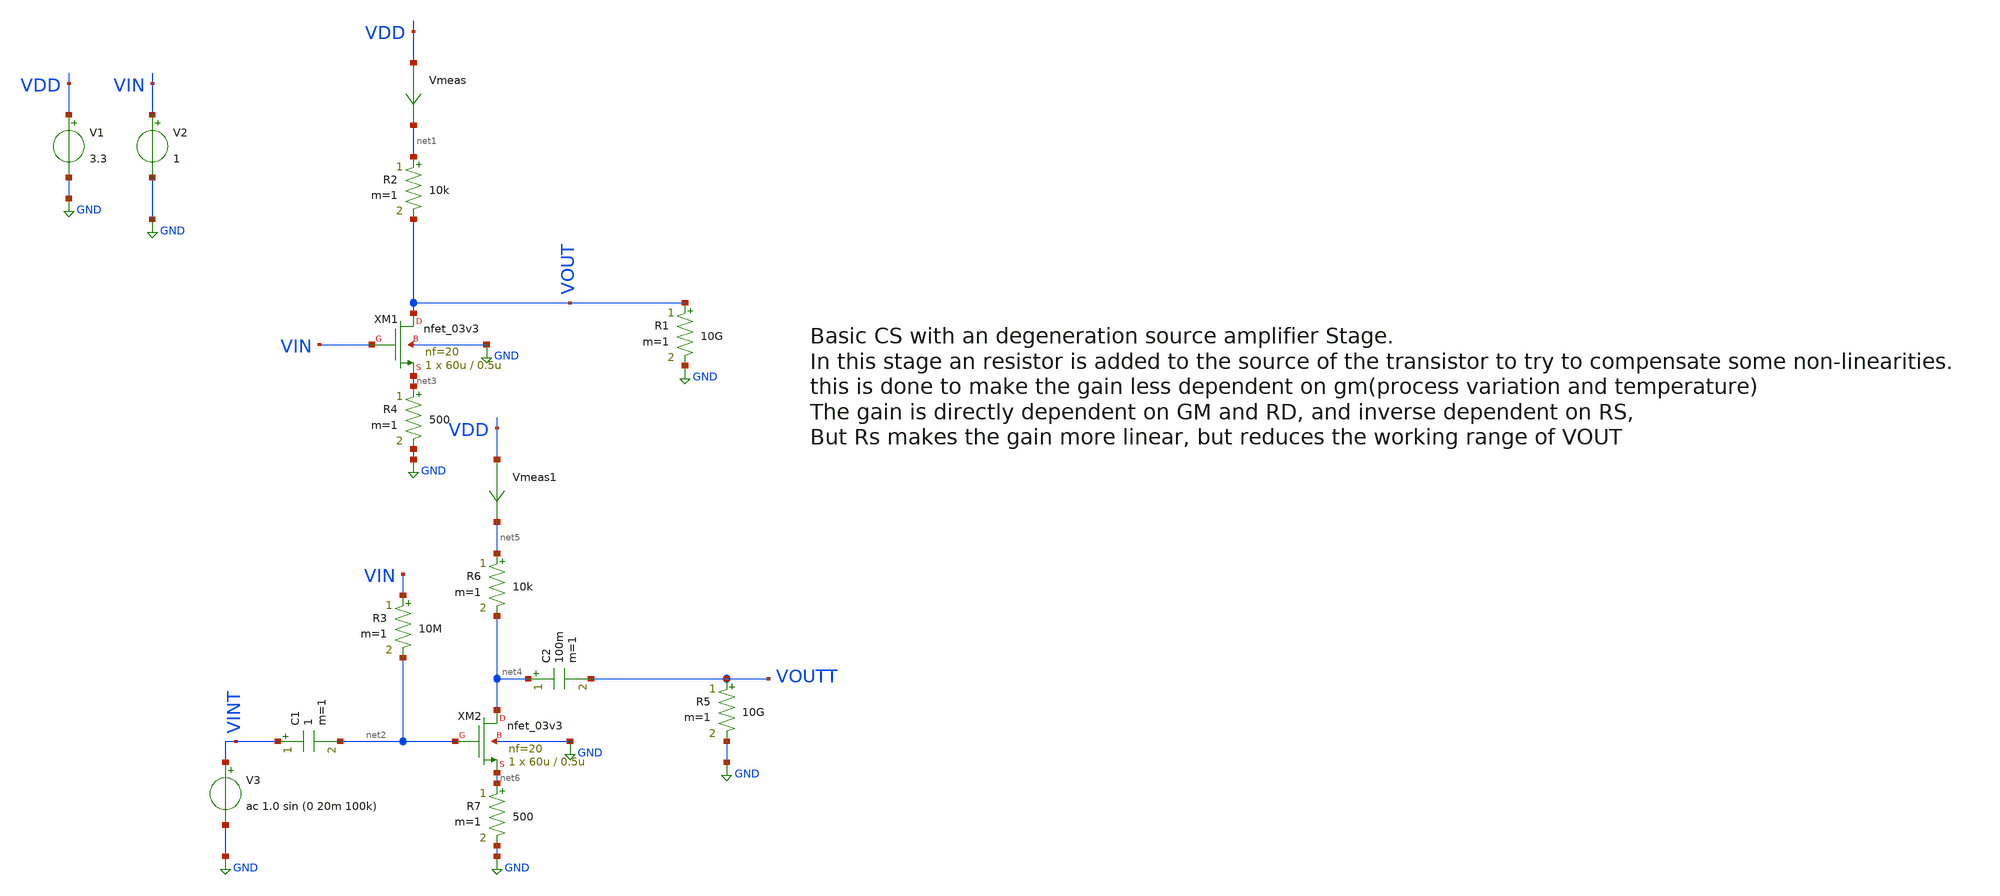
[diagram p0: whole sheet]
** sch_path: basic_circuits/cs_degenerated_source_stage.sch
**.subckt cs_degenerated_source_stage
XM1 VOUT VIN net3 GND nfet_03v3 L=0.5u W=60u nf=20 ad='int((nf+1)/2) * W/nf * 0.18u' as='int((nf+2)/2) * W/nf * 0.18u'
+ pd='2*int((nf+1)/2) * (W/nf + 0.18u)' ps='2*int((nf+2)/2) * (W/nf + 0.18u)' nrd='0.18u / W' nrs='0.18u / W'
+ sa=0 sb=0 sd=0 m=1
Vmeas VDD net1 0
.save i(vmeas)
V1 VDD GND 3.3
V2 VIN GND 1
V3 VINT GND ac 1.0 sin (0 20m 100k)
R3 VIN net2 10M m=1
R5 VOUTT GND 10G m=1
R1 VOUT GND 10G m=1
C1 VINT net2 1 m=1
R2 net1 VOUT 10k m=1
R4 net3 GND 500 m=1
XM2 net4 net2 net6 GND nfet_03v3 L=0.5u W=60u nf=20 ad='int((nf+1)/2) * W/nf * 0.18u' as='int((nf+2)/2) * W/nf * 0.18u'
+ pd='2*int((nf+1)/2) * (W/nf + 0.18u)' ps='2*int((nf+2)/2) * (W/nf + 0.18u)' nrd='0.18u / W' nrs='0.18u / W'
+ sa=0 sb=0 sd=0 m=1
Vmeas1 VDD net5 0
.save i(vmeas1)
R6 net5 net4 10k m=1
R7 net6 GND 500 m=1
C2 net4 VOUTT 100m m=1
**** begin user architecture code

**************************************************************
**************************************************************
**************************************************************
**************************************************************
**************************************************************
*LIBs*********************************************************
**************************************************************
**************************************************************
**************************************************************
**************************************************************
**************************************************************
.include $::180MCU_MODELS/design.ngspice
*.lib $::180MCU_MODELS/sm141064.ngspice statistical *use statistical if you want global and parameter mismatch
*.lib $::180MCU_MODELS/sm141064.ngspice res_statistical
.lib $::180MCU_MODELS/sm141064.ngspice typical
.lib $::180MCU_MODELS/sm141064.ngspice res_typical
.lib $::180MCU_MODELS/sm141064.ngspice moscap_typical
.lib $::180MCU_MODELS/sm141064.ngspice bjt_typical
.lib $::180MCU_MODELS/sm141064.ngspice diode_typical
.lib $::180MCU_MODELS/sm141064.ngspice mimcap_typical
**************************************************************
**************************************************************
**************************************************************
**************************************************************
**************************************************************
*Corners/montecarlo options***********************************
**************************************************************
**************************************************************
**************************************************************
**************************************************************
**************************************************************
.TEMP 27
.param   sw_stat_global = 1   sw_stat_mism = 1  mc_skew = 3  res_mc_skew = 3  cap_mc_skew = 3
+  fnoicor = 1
**************************************************************
**************************************************************
**************************************************************
**************************************************************
*SIMULATION and Plots*****************************************
**************************************************************
**************************************************************
**************************************************************
**************************************************************
.control
save all
dc V2 0 3.3 0.01
*dc simulation
plot v(VOUT) v(VIN) deriv(v(VOUT))
*ploting VIN VOUT and the voltage gain
plot i(Vmeas)
*ploting the current for curiosity
tran 1ns 20u
*transient simulation
plot (v(VINT)) (v(VOUTT))
*simple plot to exemplify the gain
fft v(VOUTT) v(VINT)
*fast fourier transfor
plot mag(v(VOUTT)) mag(v(VINT))
* analyse the frequency spectrum of the transient waves, to detect distortion
ac dec 20 1 50G
*simple ac simulation
plot v(VOUTT)
*gain in function of the input frequency
.endc

**** end user architecture code
**.ends
.GLOBAL GND
.end
